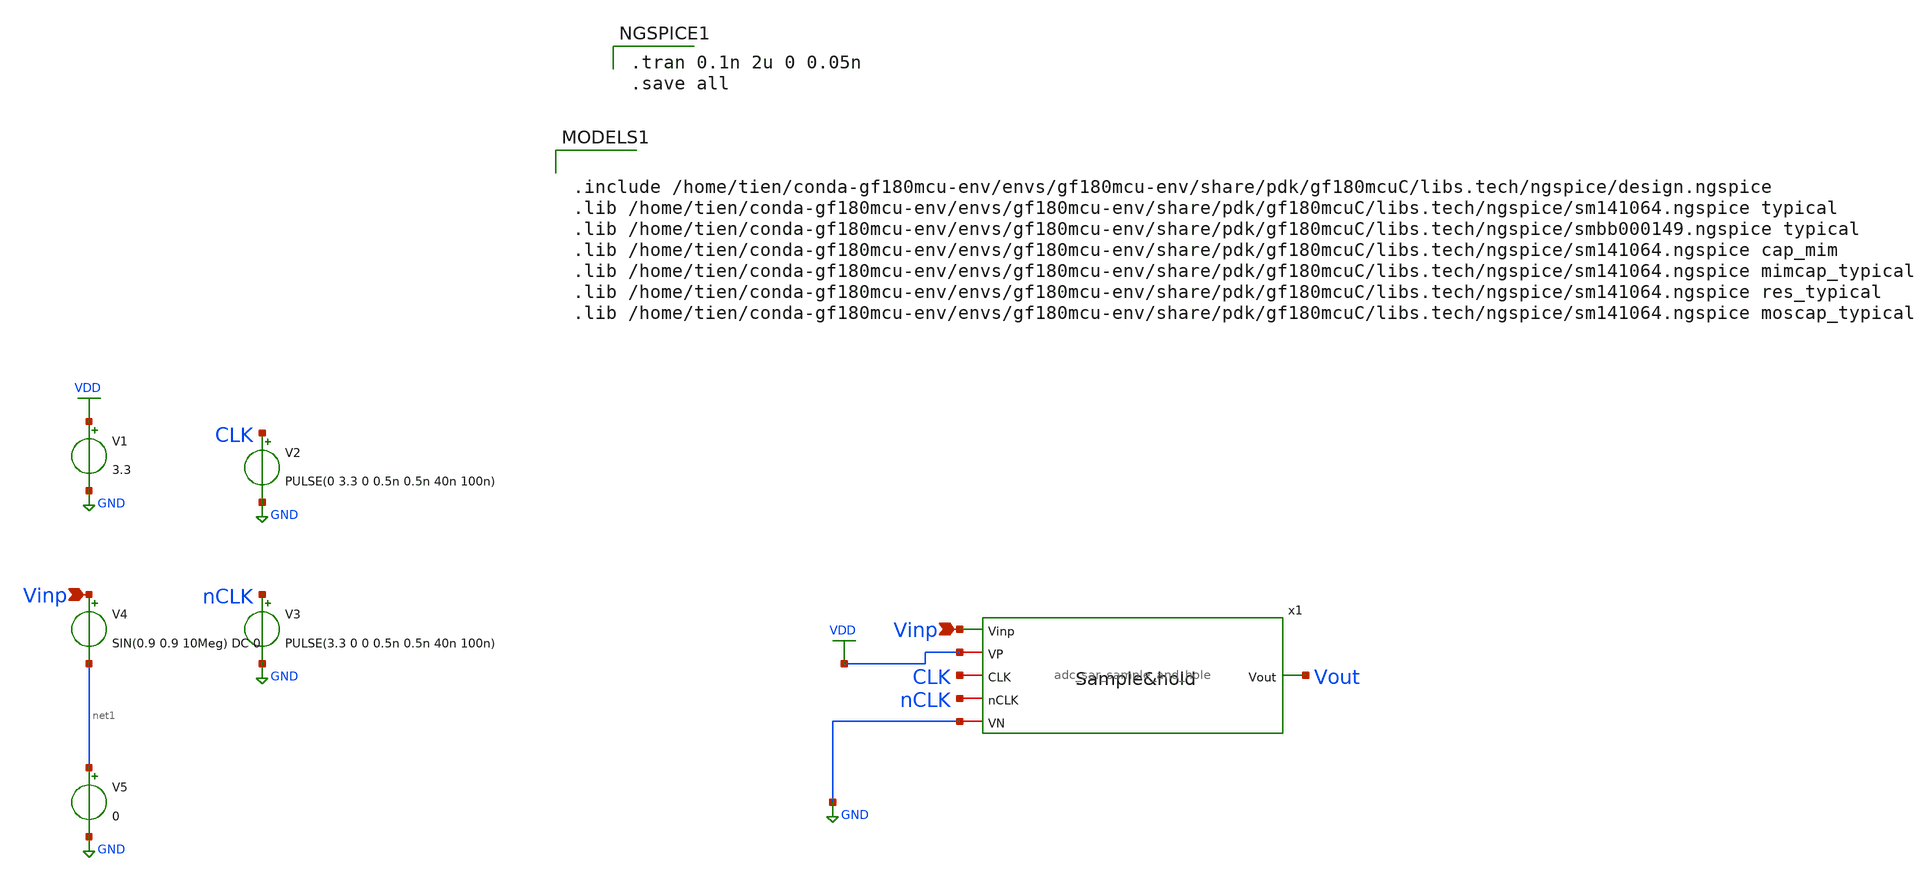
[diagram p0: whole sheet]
** sch_path: adc_sar_sample_and_hole_tb.sch
**.subckt adc_sar_sample_and_hole_tb Vinp Vinp
*.ipin Vinp
*.ipin Vinp
V1 VDD GND 3.3
V2 CLK GND PULSE(0 3.3 0 0.5n 0.5n 40n 100n)

V3 nCLK GND PULSE(3.3 0 0 0.5n 0.5n 40n 100n)

V4 Vinp net1 SIN(0.9 0.9 10Meg) DC 0
V5 net1 GND 0
x1 VDD CLK Vout nCLK Vinp GND adc_sar_sample_and_hole
**** begin user architecture code

.tran 0.1n 2u 0 0.05n
.save all



.include /home/tien/conda-gf180mcu-env/envs/gf180mcu-env/share/pdk/gf180mcuC/libs.tech/ngspice/design.ngspice
.lib /home/tien/conda-gf180mcu-env/envs/gf180mcu-env/share/pdk/gf180mcuC/libs.tech/ngspice/sm141064.ngspice typical
.lib /home/tien/conda-gf180mcu-env/envs/gf180mcu-env/share/pdk/gf180mcuC/libs.tech/ngspice/smbb000149.ngspice typical
.lib /home/tien/conda-gf180mcu-env/envs/gf180mcu-env/share/pdk/gf180mcuC/libs.tech/ngspice/sm141064.ngspice cap_mim
.lib /home/tien/conda-gf180mcu-env/envs/gf180mcu-env/share/pdk/gf180mcuC/libs.tech/ngspice/sm141064.ngspice mimcap_typical
.lib /home/tien/conda-gf180mcu-env/envs/gf180mcu-env/share/pdk/gf180mcuC/libs.tech/ngspice/sm141064.ngspice res_typical
.lib /home/tien/conda-gf180mcu-env/envs/gf180mcu-env/share/pdk/gf180mcuC/libs.tech/ngspice/sm141064.ngspice moscap_typical

**** end user architecture code
**.ends

* expanding   symbol:  adc_sar_sample_and_hole.sym # of pins=6
** sym_path: adc_sar_sample_and_hole.sym
** sch_path: adc_sar_sample_and_hole.sch
.subckt adc_sar_sample_and_hole VP CLK Vout nCLK Vinp VN
*.ipin Vinp
*.opin Vout
*.iopin VP
*.iopin CLK
*.iopin nCLK
*.iopin VN
XM1 net4 CLK VP VP pfet_03v3 L=0.28u W=0.22u nf=1 ad='int((nf+1)/2) * W/nf * 0.18u' as='int((nf+2)/2) * W/nf * 0.18u'
+ pd='2*int((nf+1)/2) * (W/nf + 0.18u)' ps='2*int((nf+2)/2) * (W/nf + 0.18u)' nrd='0.18u / W' nrs='0.18u / W'
+ sa=0 sb=0 sd=0 m=1
XM2 VP net2 net1 net1 pfet_03v3 L=0.28u W=0.22u nf=1 ad='int((nf+1)/2) * W/nf * 0.18u' as='int((nf+2)/2) * W/nf * 0.18u'
+ pd='2*int((nf+1)/2) * (W/nf + 0.18u)' ps='2*int((nf+2)/2) * (W/nf + 0.18u)' nrd='0.18u / W' nrs='0.18u / W'
+ sa=0 sb=0 sd=0 m=1
XM3 net2 net4 net1 net1 pfet_03v3 L=0.28u W=0.22u nf=1 ad='int((nf+1)/2) * W/nf * 0.18u' as='int((nf+2)/2) * W/nf * 0.18u'
+ pd='2*int((nf+1)/2) * (W/nf + 0.18u)' ps='2*int((nf+2)/2) * (W/nf + 0.18u)' nrd='0.18u / W' nrs='0.18u / W'
+ sa=0 sb=0 sd=0 m=1
XM4 net2 VP net3 VN nfet_03v3 L=0.28u W=0.22u nf=1 ad='int((nf+1)/2) * W/nf * 0.18u' as='int((nf+2)/2) * W/nf * 0.18u'
+ pd='2*int((nf+1)/2) * (W/nf + 0.18u)' ps='2*int((nf+2)/2) * (W/nf + 0.18u)' nrd='0.18u / W' nrs='0.18u / W'
+ sa=0 sb=0 sd=0 m=1
XM5 net3 nCLK VN VN nfet_03v3 L=0.28u W=0.22u nf=1 ad='int((nf+1)/2) * W/nf * 0.18u' as='int((nf+2)/2) * W/nf * 0.18u'
+ pd='2*int((nf+1)/2) * (W/nf + 0.18u)' ps='2*int((nf+2)/2) * (W/nf + 0.18u)' nrd='0.18u / W' nrs='0.18u / W'
+ sa=0 sb=0 sd=0 m=1
XM6 net4 CLK net5 VN nfet_03v3 L=0.28u W=0.22u nf=1 ad='int((nf+1)/2) * W/nf * 0.18u' as='int((nf+2)/2) * W/nf * 0.18u'
+ pd='2*int((nf+1)/2) * (W/nf + 0.18u)' ps='2*int((nf+2)/2) * (W/nf + 0.18u)' nrd='0.18u / W' nrs='0.18u / W'
+ sa=0 sb=0 sd=0 m=1
XM7 net4 net2 net5 VN nfet_03v3 L=0.28u W=0.22u nf=1 ad='int((nf+1)/2) * W/nf * 0.18u' as='int((nf+2)/2) * W/nf * 0.18u'
+ pd='2*int((nf+1)/2) * (W/nf + 0.18u)' ps='2*int((nf+2)/2) * (W/nf + 0.18u)' nrd='0.18u / W' nrs='0.18u / W'
+ sa=0 sb=0 sd=0 m=1
XM8 Vinp net2 net5 VN nfet_03v3 L=0.28u W=0.22u nf=1 ad='int((nf+1)/2) * W/nf * 0.18u' as='int((nf+2)/2) * W/nf * 0.18u'
+ pd='2*int((nf+1)/2) * (W/nf + 0.18u)' ps='2*int((nf+2)/2) * (W/nf + 0.18u)' nrd='0.18u / W' nrs='0.18u / W'
+ sa=0 sb=0 sd=0 m=1
XM9 Vout net2 Vinp VN nfet_03v3 L=0.28u W=0.39u nf=1 ad='int((nf+1)/2) * W/nf * 0.18u' as='int((nf+2)/2) * W/nf * 0.18u'
+ pd='2*int((nf+1)/2) * (W/nf + 0.18u)' ps='2*int((nf+2)/2) * (W/nf + 0.18u)' nrd='0.18u / W' nrs='0.18u / W'
+ sa=0 sb=0 sd=0 m=1
XC1 net1 net5 cap_mim_1f0fF c_width=100e-6 c_length=10e-6 m=1
XC2 Vout VN cap_mim_1f0fF c_width=3e-6 c_length=1e-6 m=1
XM10 net5 nCLK VN VN nfet_03v3 L=0.28u W=0.22u nf=1 ad='int((nf+1)/2) * W/nf * 0.18u' as='int((nf+2)/2) * W/nf * 0.18u'
+ pd='2*int((nf+1)/2) * (W/nf + 0.18u)' ps='2*int((nf+2)/2) * (W/nf + 0.18u)' nrd='0.18u / W' nrs='0.18u / W'
+ sa=0 sb=0 sd=0 m=1
.ends

.GLOBAL VDD
.GLOBAL GND
.end
